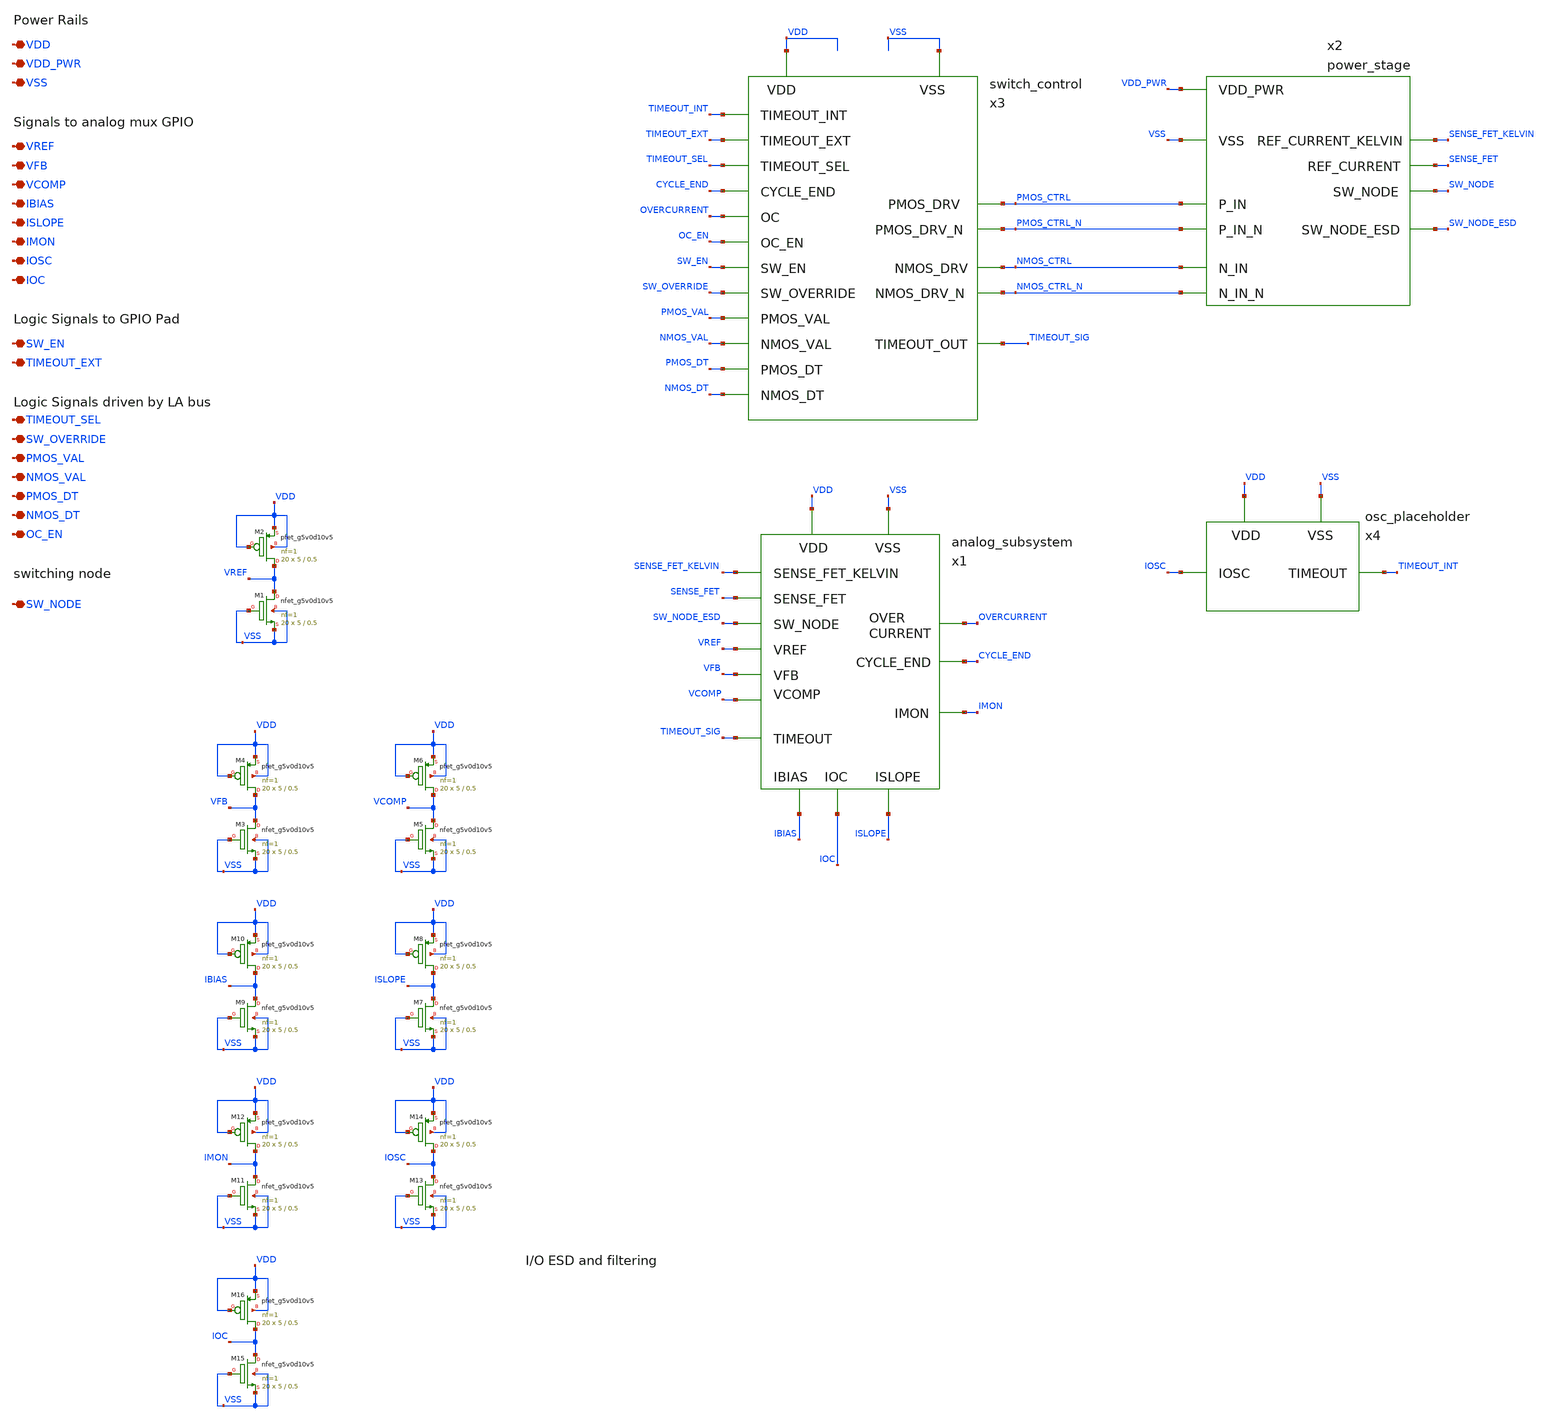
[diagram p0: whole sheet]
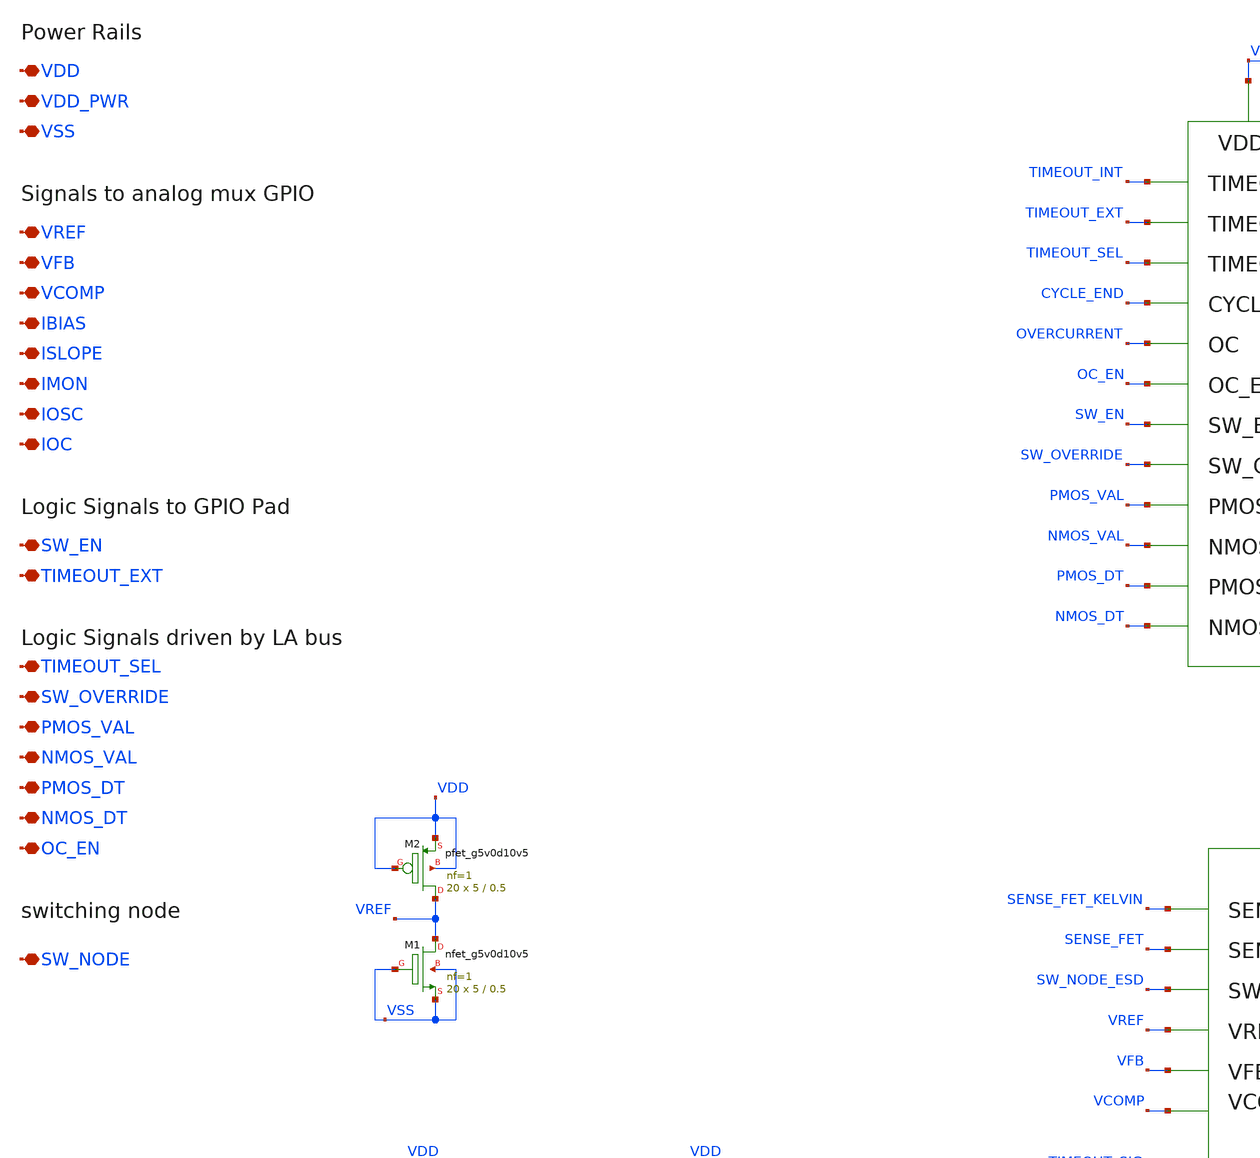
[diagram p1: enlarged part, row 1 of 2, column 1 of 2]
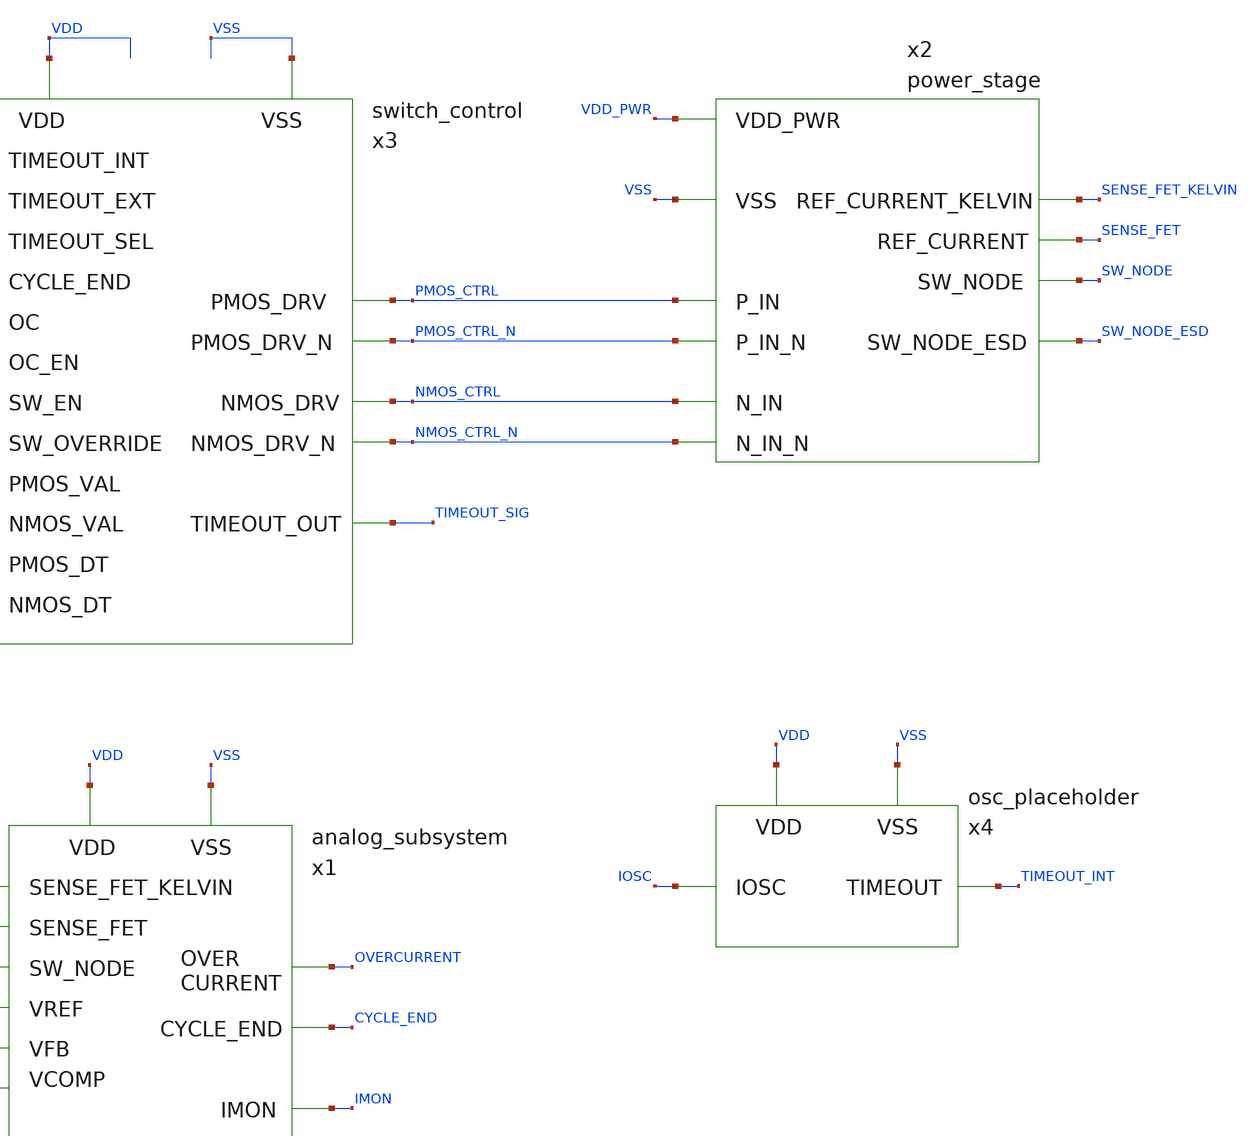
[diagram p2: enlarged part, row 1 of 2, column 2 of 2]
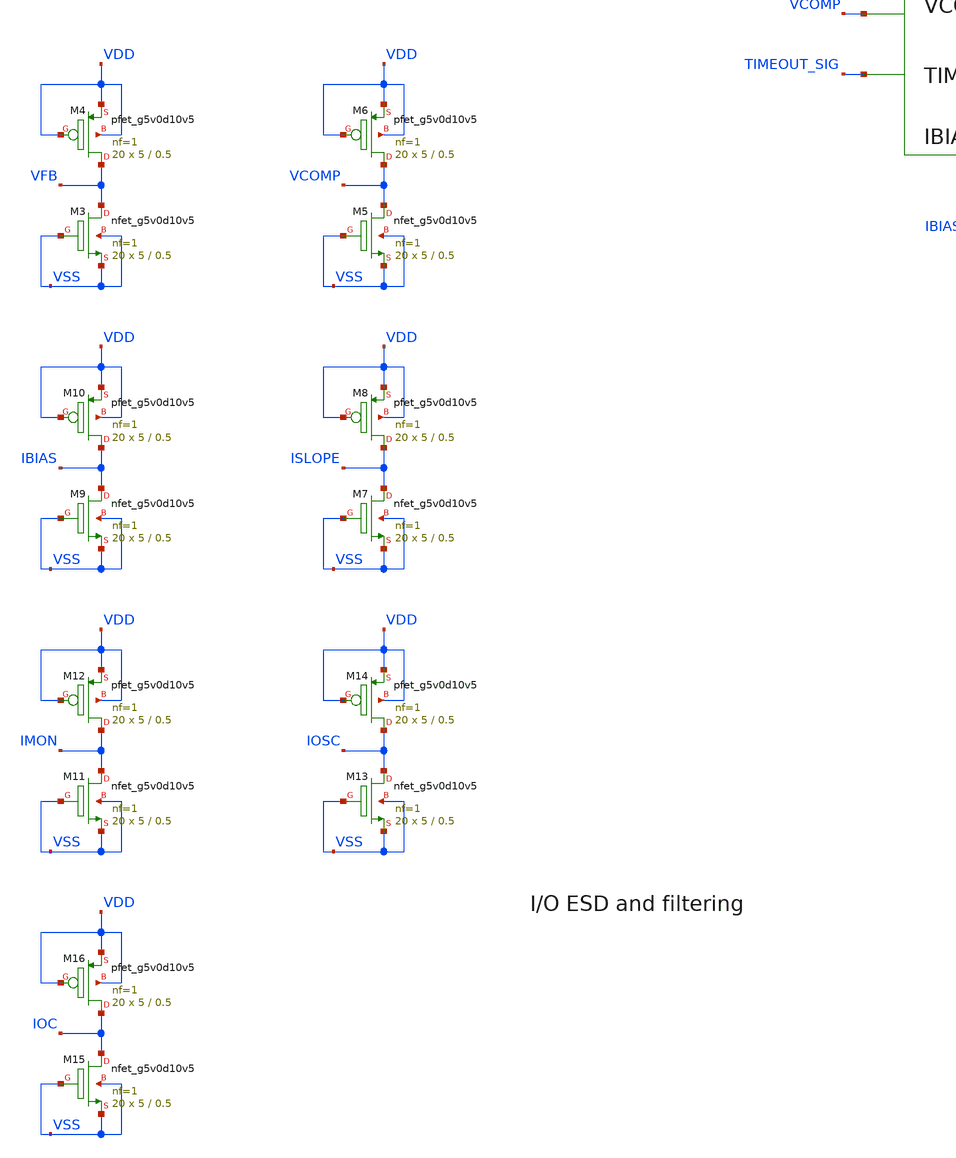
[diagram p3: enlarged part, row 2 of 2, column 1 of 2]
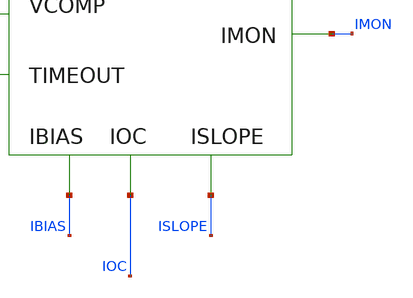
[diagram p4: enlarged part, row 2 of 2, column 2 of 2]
** sch_path: images/iic-osic-tools/addons/examples/open-pmic/design/system/full_system.sch
**.subckt full_system VDD VSS IBIAS ISLOPE VREF VFB VCOMP VDD_PWR IMON SW_EN TIMEOUT_EXT TIMEOUT_SEL
*+ SW_OVERRIDE PMOS_VAL NMOS_VAL PMOS_DT NMOS_DT IOSC SW_NODE IOC OC_EN
*.iopin VDD
*.iopin VSS
*.iopin IBIAS
*.iopin ISLOPE
*.iopin VREF
*.iopin VFB
*.iopin VCOMP
*.iopin VDD_PWR
*.iopin IMON
*.iopin SW_EN
*.iopin TIMEOUT_EXT
*.iopin TIMEOUT_SEL
*.iopin SW_OVERRIDE
*.iopin PMOS_VAL
*.iopin NMOS_VAL
*.iopin PMOS_DT
*.iopin NMOS_DT
*.iopin IOSC
*.iopin SW_NODE
*.iopin IOC
*.iopin OC_EN
x1 VDD VSS IBIAS ISLOPE SENSE_FET SW_NODE_ESD VREF VFB VCOMP TIMEOUT_SIG CYCLE_END IMON OVERCURRENT
+ IOC SENSE_FET_KELVIN analog_subsystem
x2 VDD_PWR VSS PMOS_CTRL PMOS_CTRL_N NMOS_CTRL SENSE_FET SW_NODE NMOS_CTRL_N SW_NODE_ESD
+ SENSE_FET_KELVIN power_stage
x3 CYCLE_END NMOS_CTRL NMOS_CTRL_N NMOS_DT NMOS_VAL OC_EN OVERCURRENT PMOS_CTRL PMOS_CTRL_N PMOS_DT
+ PMOS_VAL SW_EN SW_OVERRIDE TIMEOUT_EXT TIMEOUT_INT TIMEOUT_SIG TIMEOUT_SEL VDD VSS switch_control
x4 VDD VSS IOSC TIMEOUT_INT osc_placeholder
XM1 VREF VSS VSS VSS sky130_fd_pr__nfet_g5v0d10v5 L=0.5 W=5 nf=1 ad='int((nf+1)/2) * W/nf * 0.29' as='int((nf+2)/2) * W/nf * 0.29'
+ pd='2*int((nf+1)/2) * (W/nf + 0.29)' ps='2*int((nf+2)/2) * (W/nf + 0.29)' nrd='0.29 / W' nrs='0.29 / W'
+ sa=0 sb=0 sd=0 mult=20 m=20
XM2 VREF VDD VDD VDD sky130_fd_pr__pfet_g5v0d10v5 L=0.5 W=5 nf=1 ad='int((nf+1)/2) * W/nf * 0.29' as='int((nf+2)/2) * W/nf * 0.29'
+ pd='2*int((nf+1)/2) * (W/nf + 0.29)' ps='2*int((nf+2)/2) * (W/nf + 0.29)' nrd='0.29 / W' nrs='0.29 / W'
+ sa=0 sb=0 sd=0 mult=20 m=20
XM3 VFB VSS VSS VSS sky130_fd_pr__nfet_g5v0d10v5 L=0.5 W=5 nf=1 ad='int((nf+1)/2) * W/nf * 0.29' as='int((nf+2)/2) * W/nf * 0.29'
+ pd='2*int((nf+1)/2) * (W/nf + 0.29)' ps='2*int((nf+2)/2) * (W/nf + 0.29)' nrd='0.29 / W' nrs='0.29 / W'
+ sa=0 sb=0 sd=0 mult=20 m=20
XM4 VFB VDD VDD VDD sky130_fd_pr__pfet_g5v0d10v5 L=0.5 W=5 nf=1 ad='int((nf+1)/2) * W/nf * 0.29' as='int((nf+2)/2) * W/nf * 0.29'
+ pd='2*int((nf+1)/2) * (W/nf + 0.29)' ps='2*int((nf+2)/2) * (W/nf + 0.29)' nrd='0.29 / W' nrs='0.29 / W'
+ sa=0 sb=0 sd=0 mult=20 m=20
XM5 VCOMP VSS VSS VSS sky130_fd_pr__nfet_g5v0d10v5 L=0.5 W=5 nf=1 ad='int((nf+1)/2) * W/nf * 0.29' as='int((nf+2)/2) * W/nf * 0.29'
+ pd='2*int((nf+1)/2) * (W/nf + 0.29)' ps='2*int((nf+2)/2) * (W/nf + 0.29)' nrd='0.29 / W' nrs='0.29 / W'
+ sa=0 sb=0 sd=0 mult=20 m=20
XM6 VCOMP VDD VDD VDD sky130_fd_pr__pfet_g5v0d10v5 L=0.5 W=5 nf=1 ad='int((nf+1)/2) * W/nf * 0.29' as='int((nf+2)/2) * W/nf * 0.29'
+ pd='2*int((nf+1)/2) * (W/nf + 0.29)' ps='2*int((nf+2)/2) * (W/nf + 0.29)' nrd='0.29 / W' nrs='0.29 / W'
+ sa=0 sb=0 sd=0 mult=20 m=20
XM7 ISLOPE VSS VSS VSS sky130_fd_pr__nfet_g5v0d10v5 L=0.5 W=5 nf=1 ad='int((nf+1)/2) * W/nf * 0.29' as='int((nf+2)/2) * W/nf * 0.29'
+ pd='2*int((nf+1)/2) * (W/nf + 0.29)' ps='2*int((nf+2)/2) * (W/nf + 0.29)' nrd='0.29 / W' nrs='0.29 / W'
+ sa=0 sb=0 sd=0 mult=20 m=20
XM8 ISLOPE VDD VDD VDD sky130_fd_pr__pfet_g5v0d10v5 L=0.5 W=5 nf=1 ad='int((nf+1)/2) * W/nf * 0.29' as='int((nf+2)/2) * W/nf * 0.29'
+ pd='2*int((nf+1)/2) * (W/nf + 0.29)' ps='2*int((nf+2)/2) * (W/nf + 0.29)' nrd='0.29 / W' nrs='0.29 / W'
+ sa=0 sb=0 sd=0 mult=20 m=20
XM9 IBIAS VSS VSS VSS sky130_fd_pr__nfet_g5v0d10v5 L=0.5 W=5 nf=1 ad='int((nf+1)/2) * W/nf * 0.29' as='int((nf+2)/2) * W/nf * 0.29'
+ pd='2*int((nf+1)/2) * (W/nf + 0.29)' ps='2*int((nf+2)/2) * (W/nf + 0.29)' nrd='0.29 / W' nrs='0.29 / W'
+ sa=0 sb=0 sd=0 mult=20 m=20
XM10 IBIAS VDD VDD VDD sky130_fd_pr__pfet_g5v0d10v5 L=0.5 W=5 nf=1 ad='int((nf+1)/2) * W/nf * 0.29' as='int((nf+2)/2) * W/nf * 0.29'
+ pd='2*int((nf+1)/2) * (W/nf + 0.29)' ps='2*int((nf+2)/2) * (W/nf + 0.29)' nrd='0.29 / W' nrs='0.29 / W'
+ sa=0 sb=0 sd=0 mult=20 m=20
XM11 IMON VSS VSS VSS sky130_fd_pr__nfet_g5v0d10v5 L=0.5 W=5 nf=1 ad='int((nf+1)/2) * W/nf * 0.29' as='int((nf+2)/2) * W/nf * 0.29'
+ pd='2*int((nf+1)/2) * (W/nf + 0.29)' ps='2*int((nf+2)/2) * (W/nf + 0.29)' nrd='0.29 / W' nrs='0.29 / W'
+ sa=0 sb=0 sd=0 mult=20 m=20
XM12 IMON VDD VDD VDD sky130_fd_pr__pfet_g5v0d10v5 L=0.5 W=5 nf=1 ad='int((nf+1)/2) * W/nf * 0.29' as='int((nf+2)/2) * W/nf * 0.29'
+ pd='2*int((nf+1)/2) * (W/nf + 0.29)' ps='2*int((nf+2)/2) * (W/nf + 0.29)' nrd='0.29 / W' nrs='0.29 / W'
+ sa=0 sb=0 sd=0 mult=20 m=20
XM13 IOSC VSS VSS VSS sky130_fd_pr__nfet_g5v0d10v5 L=0.5 W=5 nf=1 ad='int((nf+1)/2) * W/nf * 0.29' as='int((nf+2)/2) * W/nf * 0.29'
+ pd='2*int((nf+1)/2) * (W/nf + 0.29)' ps='2*int((nf+2)/2) * (W/nf + 0.29)' nrd='0.29 / W' nrs='0.29 / W'
+ sa=0 sb=0 sd=0 mult=20 m=20
XM14 IOSC VDD VDD VDD sky130_fd_pr__pfet_g5v0d10v5 L=0.5 W=5 nf=1 ad='int((nf+1)/2) * W/nf * 0.29' as='int((nf+2)/2) * W/nf * 0.29'
+ pd='2*int((nf+1)/2) * (W/nf + 0.29)' ps='2*int((nf+2)/2) * (W/nf + 0.29)' nrd='0.29 / W' nrs='0.29 / W'
+ sa=0 sb=0 sd=0 mult=20 m=20
XM15 IOC VSS VSS VSS sky130_fd_pr__nfet_g5v0d10v5 L=0.5 W=5 nf=1 ad='int((nf+1)/2) * W/nf * 0.29' as='int((nf+2)/2) * W/nf * 0.29'
+ pd='2*int((nf+1)/2) * (W/nf + 0.29)' ps='2*int((nf+2)/2) * (W/nf + 0.29)' nrd='0.29 / W' nrs='0.29 / W'
+ sa=0 sb=0 sd=0 mult=20 m=20
XM16 IOC VDD VDD VDD sky130_fd_pr__pfet_g5v0d10v5 L=0.5 W=5 nf=1 ad='int((nf+1)/2) * W/nf * 0.29' as='int((nf+2)/2) * W/nf * 0.29'
+ pd='2*int((nf+1)/2) * (W/nf + 0.29)' ps='2*int((nf+2)/2) * (W/nf + 0.29)' nrd='0.29 / W' nrs='0.29 / W'
+ sa=0 sb=0 sd=0 mult=20 m=20
**.ends
.end
